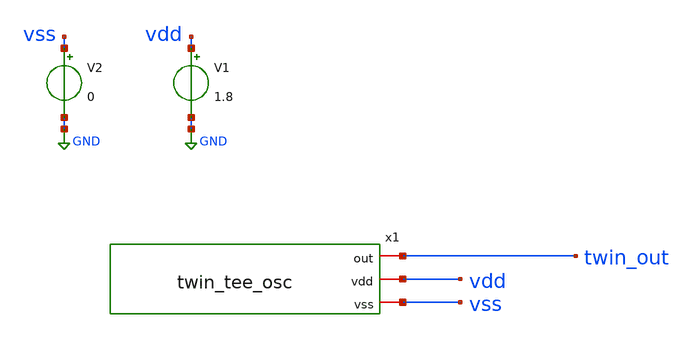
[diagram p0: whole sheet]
** sch_path: xschem/tb_twin_tee_osc.sch
**.subckt tb_twin_tee_osc
V1 vdd GND 1.8
V2 vss GND 0
x1 twin_out vdd vss twin_tee_osc
**** begin user architecture code

** opencircuitdesign pdks install
.lib $::SKYWATER_MODELS/sky130.lib.spice tt
.include $::SKYWATER_STDCELLS/sky130_fd_sc_hd.spice





.option reltol=1e-5
.param mc_mm_switch=0
.ic v(twin_out)=0.8
.control
  tran 500p 15u uic
  write tb_twin_tee_osc.raw
  set appendwrite


.endc


**** end user architecture code
**.ends

* expanding   symbol:  twin_tee_osc.sym # of pins=3
** sym_path: xschem/twin_tee_osc.sym
** sch_path: xschem/twin_tee_osc.sch
.subckt twin_tee_osc out vdd vss
*.iopin vdd
*.iopin vss
*.iopin out
x1 vdd net1 net2 out vss p3_opamp
XR1 vss net1 vss sky130_fd_pr__res_high_po_0p35 L=10 mult=1 m=1
XR3 net1 vdd vss sky130_fd_pr__res_high_po_0p35 L=10 mult=1 m=1
x2 vdd vss out net2 twin_tee
.ends


* expanding   symbol:  p3_opamp.sym # of pins=5
** sym_path: p3_opamp.sym
** sch_path: p3_opamp.sch
.subckt p3_opamp VDD MINUS PLUS VOUT VSS
*.iopin VDD
*.iopin VSS
*.iopin PLUS
*.iopin MINUS
*.iopin VOUT
XM3 VX VBIAS VSS VSS sky130_fd_pr__nfet_01v8 L=2 W=4 nf=4 ad='int((nf+1)/2) * W/nf * 0.29' as='int((nf+2)/2) * W/nf * 0.29'
+ pd='2*int((nf+1)/2) * (W/nf + 0.29)' ps='2*int((nf+2)/2) * (W/nf + 0.29)' nrd='0.29 / W' nrs='0.29 / W'
+ sa=0 sb=0 sd=0 mult=1 m=1
XM6 VBIAS VBIAS VSS VSS sky130_fd_pr__nfet_01v8 L=2 W=4 nf=4 ad='int((nf+1)/2) * W/nf * 0.29' as='int((nf+2)/2) * W/nf * 0.29'
+ pd='2*int((nf+1)/2) * (W/nf + 0.29)' ps='2*int((nf+2)/2) * (W/nf + 0.29)' nrd='0.29 / W' nrs='0.29 / W'
+ sa=0 sb=0 sd=0 mult=1 m=1
XM7 VOUT VBIAS VSS VSS sky130_fd_pr__nfet_01v8 L=2 W=7 nf=7 ad='int((nf+1)/2) * W/nf * 0.29' as='int((nf+2)/2) * W/nf * 0.29'
+ pd='2*int((nf+1)/2) * (W/nf + 0.29)' ps='2*int((nf+2)/2) * (W/nf + 0.29)' nrd='0.29 / W' nrs='0.29 / W'
+ sa=0 sb=0 sd=0 mult=1 m=1
XR1 VBIAS VDD VSS sky130_fd_pr__res_xhigh_po_0p35 L=2.9 mult=1 m=1
XM2 V2 MINUS VX VSS sky130_fd_pr__nfet_01v8_lvt L=0.5 W=2.5 nf=1 ad='int((nf+1)/2) * W/nf * 0.29' as='int((nf+2)/2) * W/nf * 0.29'
+ pd='2*int((nf+1)/2) * (W/nf + 0.29)' ps='2*int((nf+2)/2) * (W/nf + 0.29)' nrd='0.29 / W' nrs='0.29 / W'
+ sa=0 sb=0 sd=0 mult=1 m=1
XM1 V1 PLUS VX VSS sky130_fd_pr__nfet_01v8_lvt L=0.5 W=2.5 nf=1 ad='int((nf+1)/2) * W/nf * 0.29' as='int((nf+2)/2) * W/nf * 0.29'
+ pd='2*int((nf+1)/2) * (W/nf + 0.29)' ps='2*int((nf+2)/2) * (W/nf + 0.29)' nrd='0.29 / W' nrs='0.29 / W'
+ sa=0 sb=0 sd=0 mult=1 m=1
XM4 V2 V2 VDD VDD sky130_fd_pr__pfet_01v8_lvt L=2 W=6 nf=6 ad='int((nf+1)/2) * W/nf * 0.29' as='int((nf+2)/2) * W/nf * 0.29'
+ pd='2*int((nf+1)/2) * (W/nf + 0.29)' ps='2*int((nf+2)/2) * (W/nf + 0.29)' nrd='0.29 / W' nrs='0.29 / W'
+ sa=0 sb=0 sd=0 mult=1 m=1
XM5 V1 V2 VDD VDD sky130_fd_pr__pfet_01v8_lvt L=2 W=6 nf=6 ad='int((nf+1)/2) * W/nf * 0.29' as='int((nf+2)/2) * W/nf * 0.29'
+ pd='2*int((nf+1)/2) * (W/nf + 0.29)' ps='2*int((nf+2)/2) * (W/nf + 0.29)' nrd='0.29 / W' nrs='0.29 / W'
+ sa=0 sb=0 sd=0 mult=1 m=1
XM8 VOUT V1 VDD VDD sky130_fd_pr__pfet_01v8_lvt L=0.5 W=20 nf=20 ad='int((nf+1)/2) * W/nf * 0.29' as='int((nf+2)/2) * W/nf * 0.29'
+ pd='2*int((nf+1)/2) * (W/nf + 0.29)' ps='2*int((nf+2)/2) * (W/nf + 0.29)' nrd='0.29 / W' nrs='0.29 / W'
+ sa=0 sb=0 sd=0 mult=1 m=1
.ends


* expanding   symbol:  twin_tee.sym # of pins=4
** sym_path: xschem/twin_tee.sym
** sch_path: xschem/twin_tee.sch
.subckt twin_tee vdd vss out in
*.iopin vdd
*.iopin vss
*.iopin in
*.iopin out
XR4 net1 out vss sky130_fd_pr__res_high_po_0p35 L=10 mult=1 m=1
XC1 net1 vss sky130_fd_pr__cap_mim_m3_1 W=15 L=15 MF=1 m=1
XC2 net1 vss sky130_fd_pr__cap_mim_m3_1 W=15 L=15 MF=1 m=1
XR5 in net1 vss sky130_fd_pr__res_high_po_0p35 L=10 mult=1 m=1
XC3 net2 in sky130_fd_pr__cap_mim_m3_1 W=15 L=15 MF=1 m=1
XC4 out net2 sky130_fd_pr__cap_mim_m3_1 W=15 L=15 MF=1 m=1
XR6 net2 vss vss sky130_fd_pr__res_high_po_0p35 L=5 mult=1 m=1
.ends

.GLOBAL GND
.end
